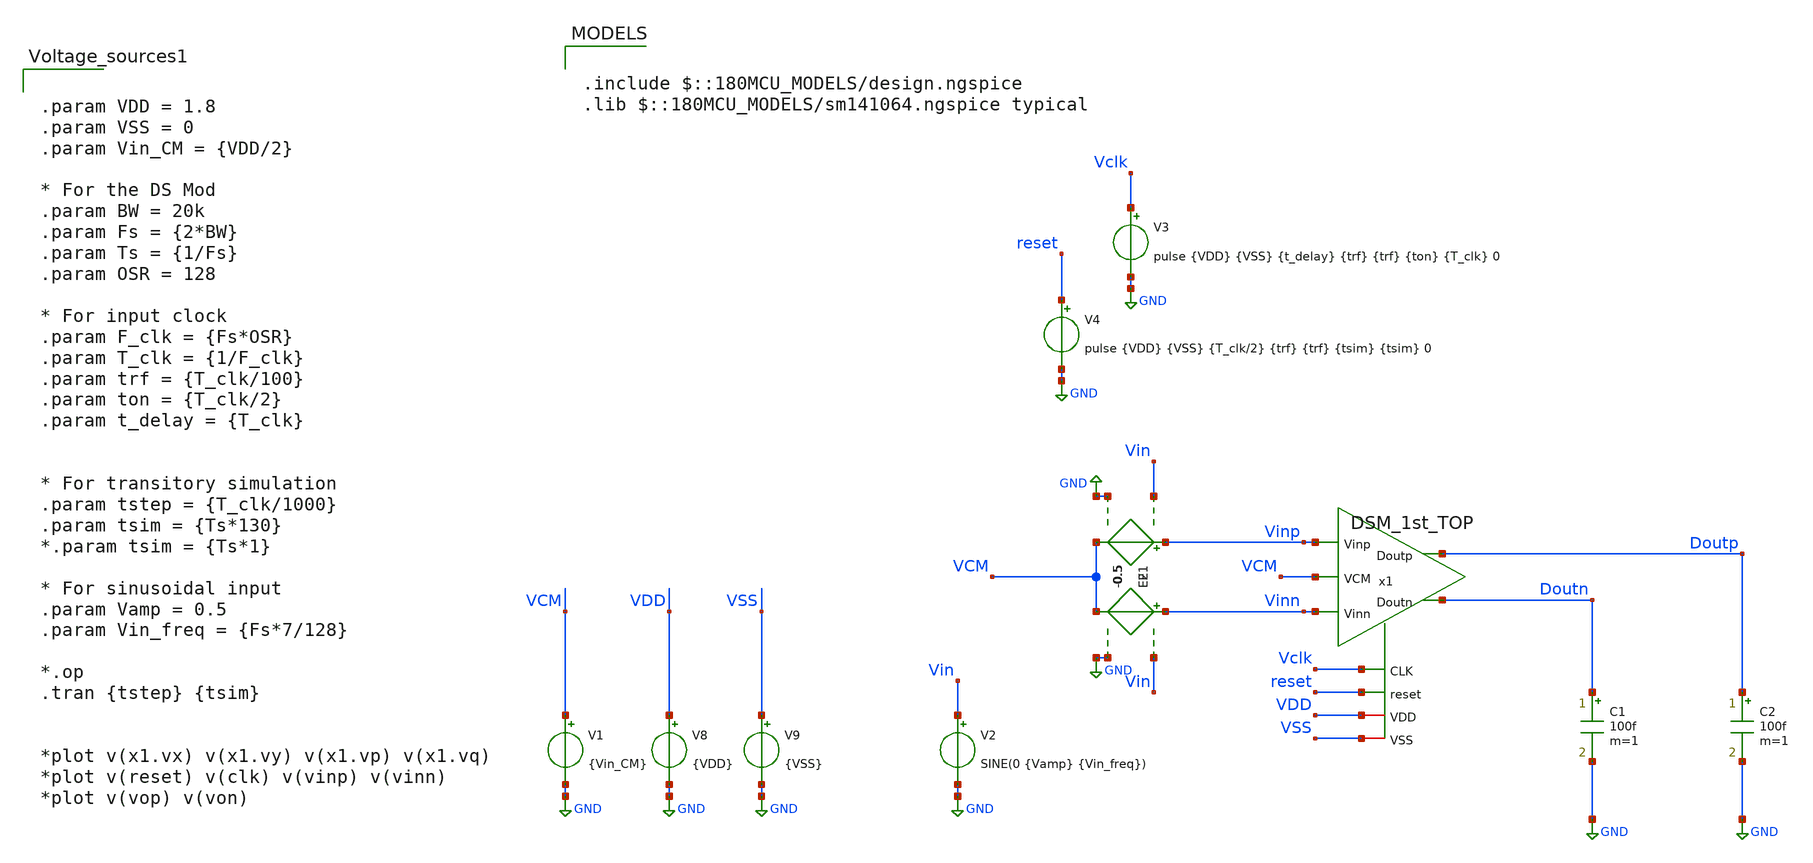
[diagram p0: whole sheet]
** sch_path: designs/DS_modulator/DSM_TOP_1or/xschem/DSM_1st_TOP_TB.sch
**.subckt DSM_1st_TOP_TB
V8 VDD GND {VDD}
V9 VSS GND {VSS}
V4 reset GND pulse {VDD} {VSS} {T_clk/2} {trf} {trf} {tsim} {tsim} 0
V3 Vclk GND pulse {VDD} {VSS} {t_delay} {trf} {trf} {ton} {T_clk} 0
C1 Doutn GND 100f m=1
C2 Doutp GND 100f m=1
V1 VCM GND {Vin_CM}
V2 Vin GND SINE(0 {Vamp} {Vin_freq})
E1 Vinp VCM Vin GND 0.5
E2 Vinn VCM Vin GND -0.5
x1 VDD VSS Doutp Vclk Vinp Vinn Doutn reset VCM DSM_1st_TOP
**** begin user architecture code

.include $::180MCU_MODELS/design.ngspice
.lib $::180MCU_MODELS/sm141064.ngspice typical



.param VDD = 1.8
.param VSS = 0
.param Vin_CM = {VDD/2}

* For the DS Mod
.param BW = 20k
.param Fs = {2*BW}
.param Ts = {1/Fs}
.param OSR = 128

* For input clock
.param F_clk = {Fs*OSR}
.param T_clk = {1/F_clk}
.param trf = {T_clk/100}
.param ton = {T_clk/2}
.param t_delay = {T_clk}


* For transitory simulation
.param tstep = {T_clk/1000}
.param tsim = {Ts*130}
*.param tsim = {Ts*1}

* For sinusoidal input
.param Vamp = 0.5
.param Vin_freq = {Fs*7/128}

*.op
.tran {tstep} {tsim}


*plot v(x1.vx) v(x1.vy) v(x1.vp) v(x1.vq)
*plot v(reset) v(clk) v(vinp) v(vinn)
*plot v(vop) v(von)






.options method=gear
.control
    save Doutp Doutn
    *save x1.Vintp_1 x1.Vintn_1 VCM x1.phi_1 x1.phi_2
    *save x1.x7.Vfx_p x1.x7.FransiscoP x1.x7.Vsp x1.x7.FransiscoP x1.Vintp_1 x1.x7.Vtp x1.phi_1
+ x1.phi_2

    * run tran simulation
    *tran 0.1u 10u
    run
    let Vout = v(Doutp)-v(Doutn)

    *plot v(Vin)
    *plot Vout
    *plot Vclk reset
    *plot x1.Vintp_1 x1.Vintn_1 VCM x1.phi_1 x1.phi_2
    *plot x1.x7.P1 x1.x7.P2
    *plot x1.x7.Vfx_p-x1.x7.FransiscoP x1.x7.Vsp-x1.x7.FransiscoP x1.Vintp_1-x1.x7.Vtp x1.phi_1
+ x1.phi_2
    *plot Vout

    *write DSM_TOP_TB.raw

    set wr_vecnames
    *wrdata DSmod_1st_data.txt Vout Vin Vinp Vinn Doutp Doutn x1.Vintp_1 x1.Vintn_1
    wrdata DSmod_1st_data_tmp.txt Vout

.endc



**** end user architecture code
**.ends
.GLOBAL GND
.end
